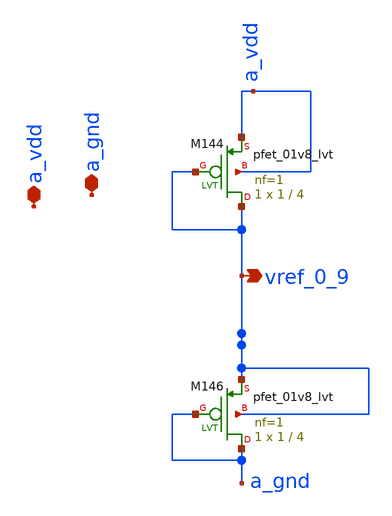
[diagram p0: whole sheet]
** sch_path: xschem/charge_pumps2/reference_0_9.sch
**.subckt reference_0_9 a_vdd a_gnd vref_0_9
*.iopin a_vdd
*.iopin a_gnd
*.opin vref_0_9
XM144 vref_0_9 vref_0_9 a_vdd a_vdd sky130_fd_pr__pfet_01v8_lvt L=4 W=1 nf=1 ad='int((nf+1)/2) * W/nf * 0.29'
+ as='int((nf+2)/2) * W/nf * 0.29' pd='2*int((nf+1)/2) * (W/nf + 0.29)' ps='2*int((nf+2)/2) * (W/nf + 0.29)'
+ nrd='0.29 / W' nrs='0.29 / W' sa=0 sb=0 sd=0 mult=1 m=1
XM146 a_gnd a_gnd vref_0_9 vref_0_9 sky130_fd_pr__pfet_01v8_lvt L=4 W=1 nf=1 ad='int((nf+1)/2) * W/nf * 0.29'
+ as='int((nf+2)/2) * W/nf * 0.29' pd='2*int((nf+1)/2) * (W/nf + 0.29)' ps='2*int((nf+2)/2) * (W/nf + 0.29)'
+ nrd='0.29 / W' nrs='0.29 / W' sa=0 sb=0 sd=0 mult=1 m=1
**.ends
.end
